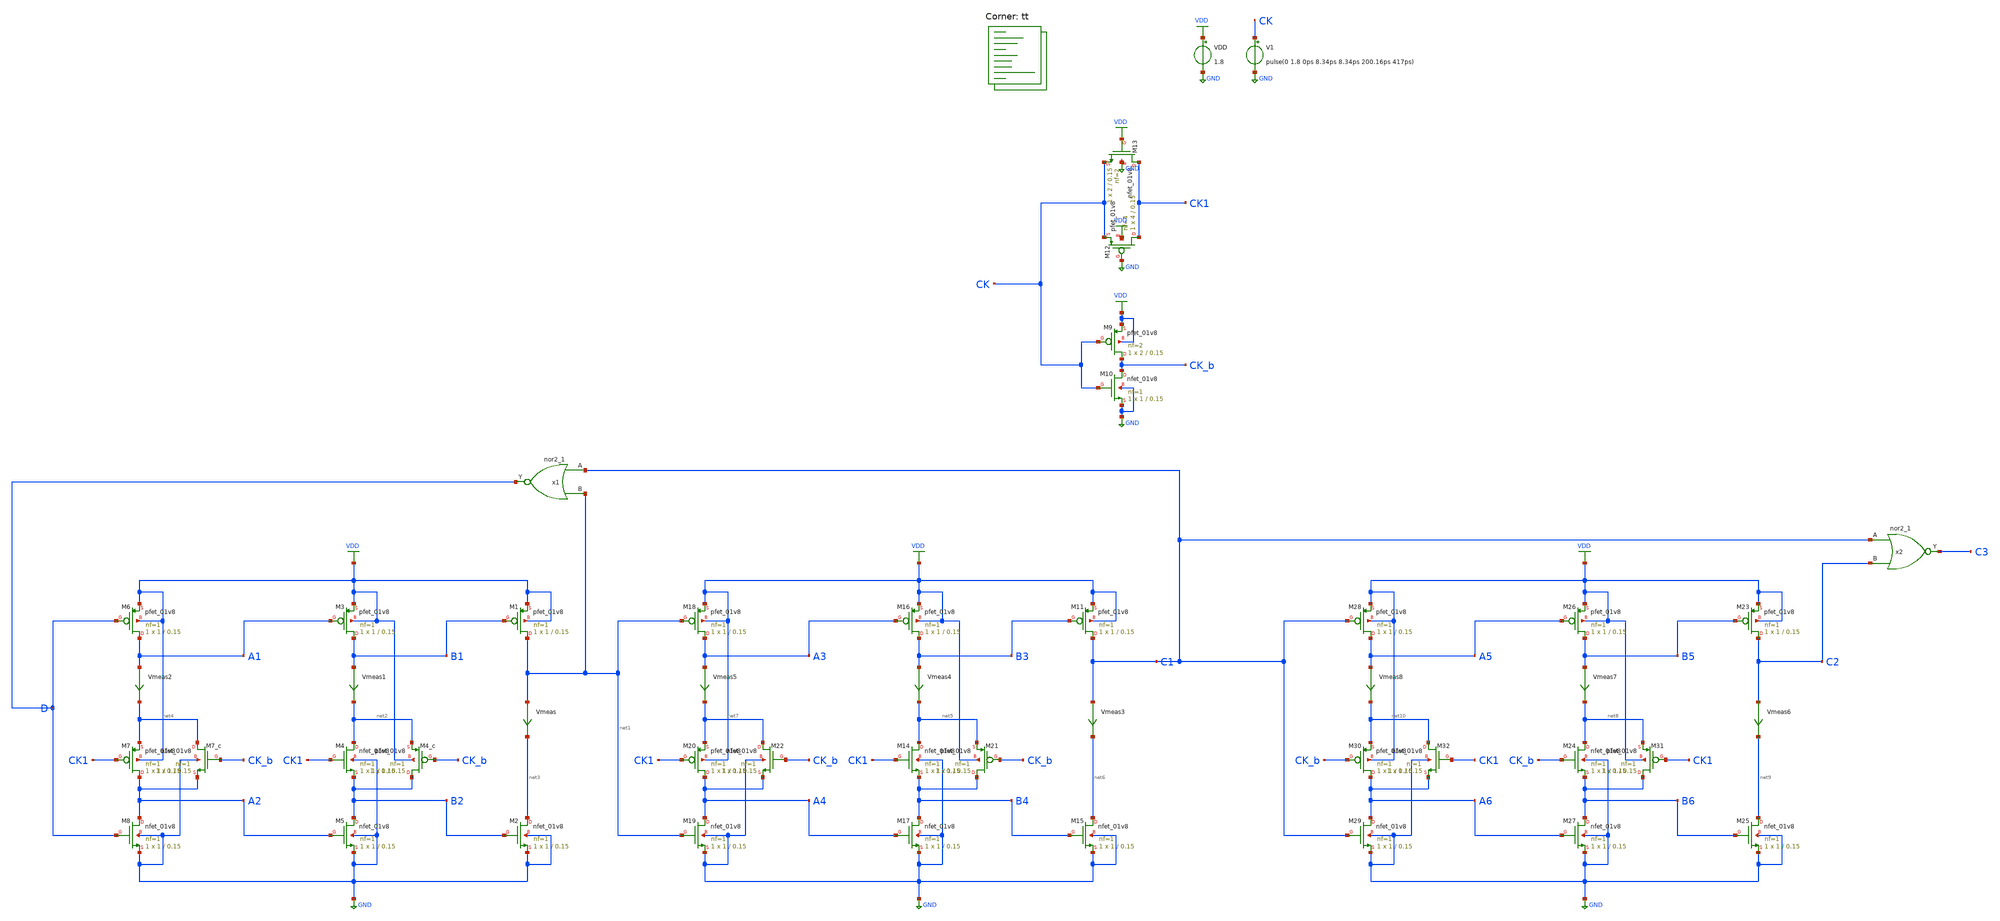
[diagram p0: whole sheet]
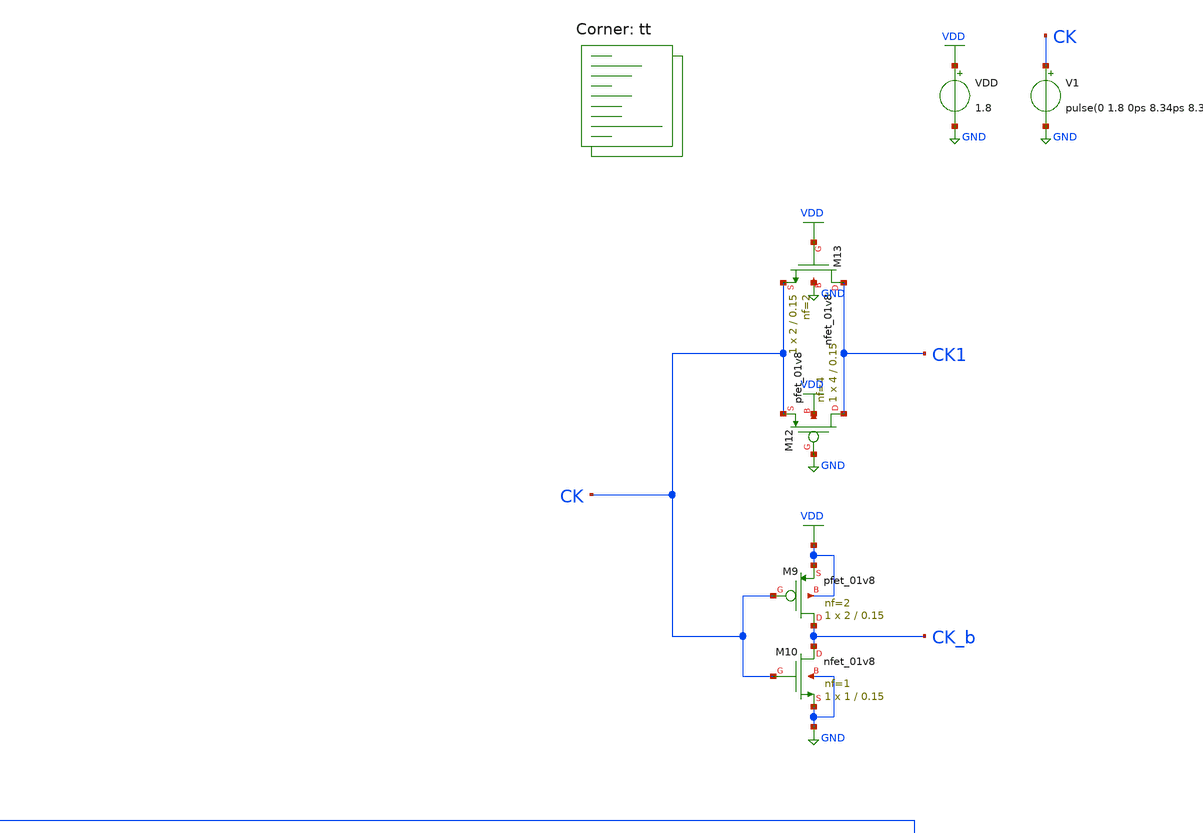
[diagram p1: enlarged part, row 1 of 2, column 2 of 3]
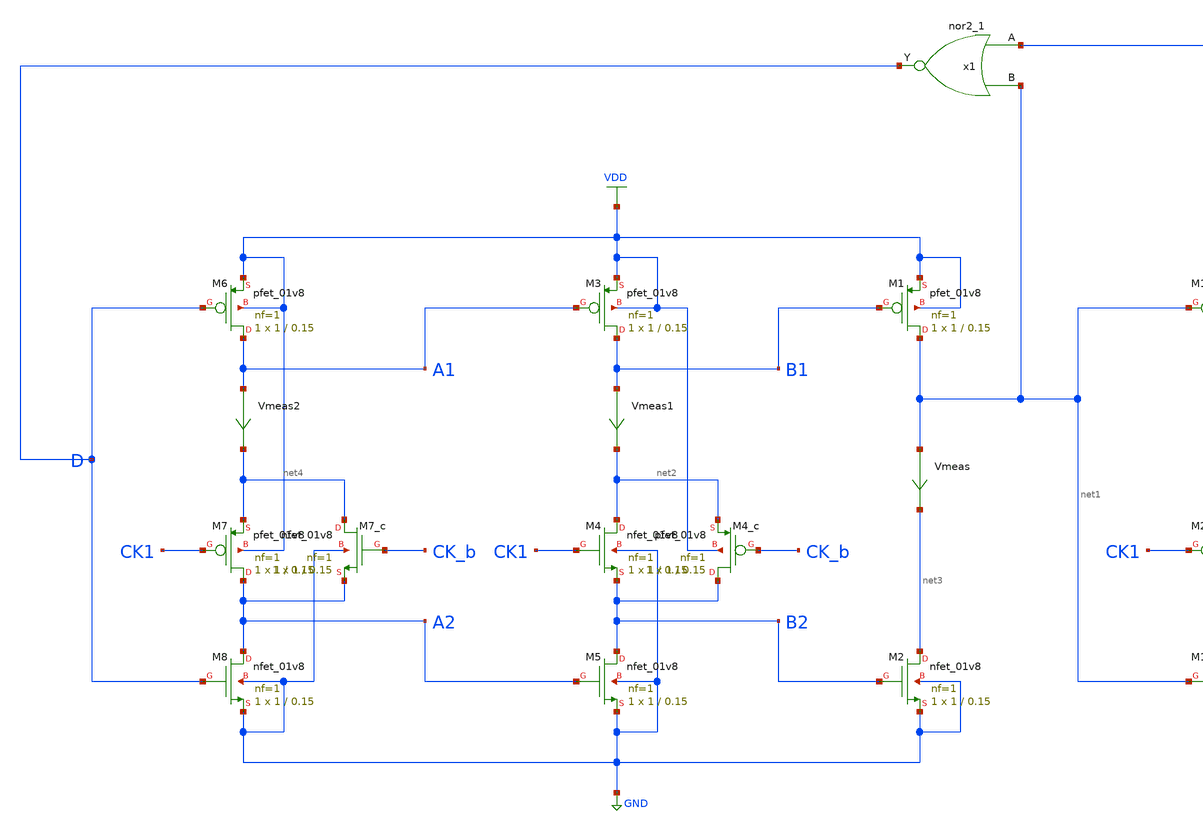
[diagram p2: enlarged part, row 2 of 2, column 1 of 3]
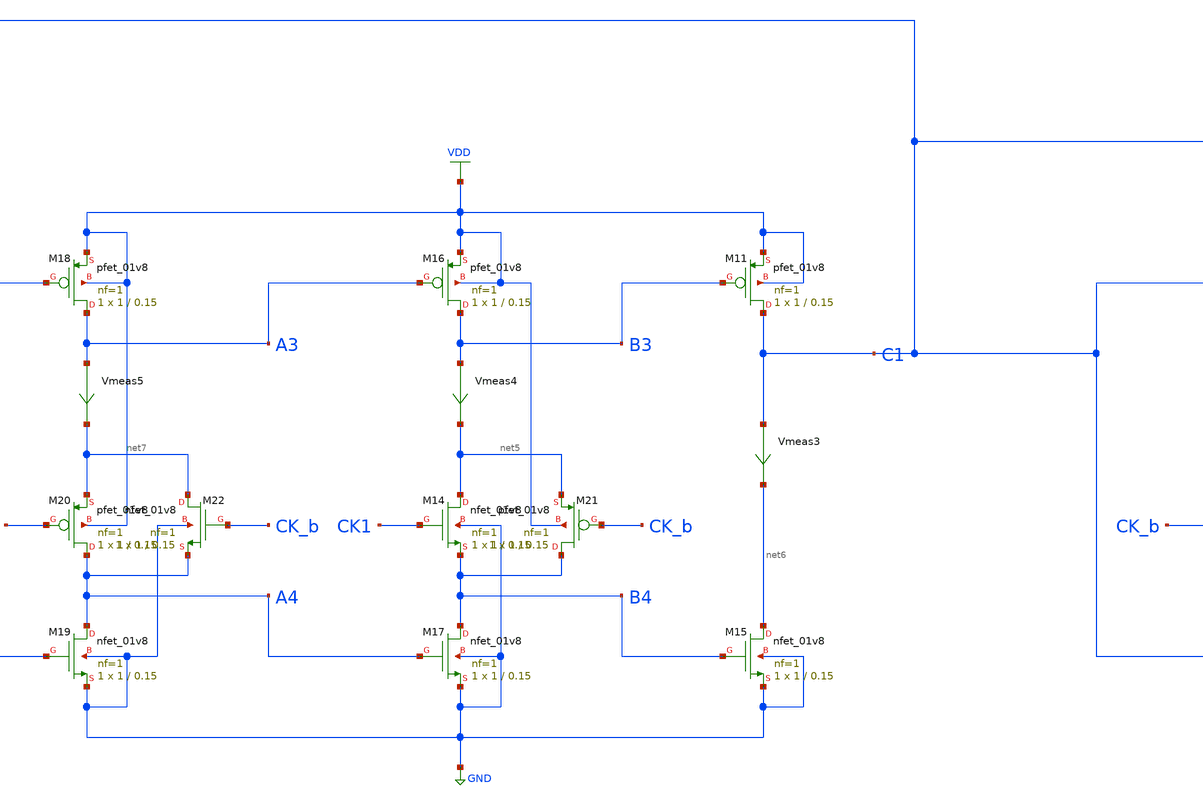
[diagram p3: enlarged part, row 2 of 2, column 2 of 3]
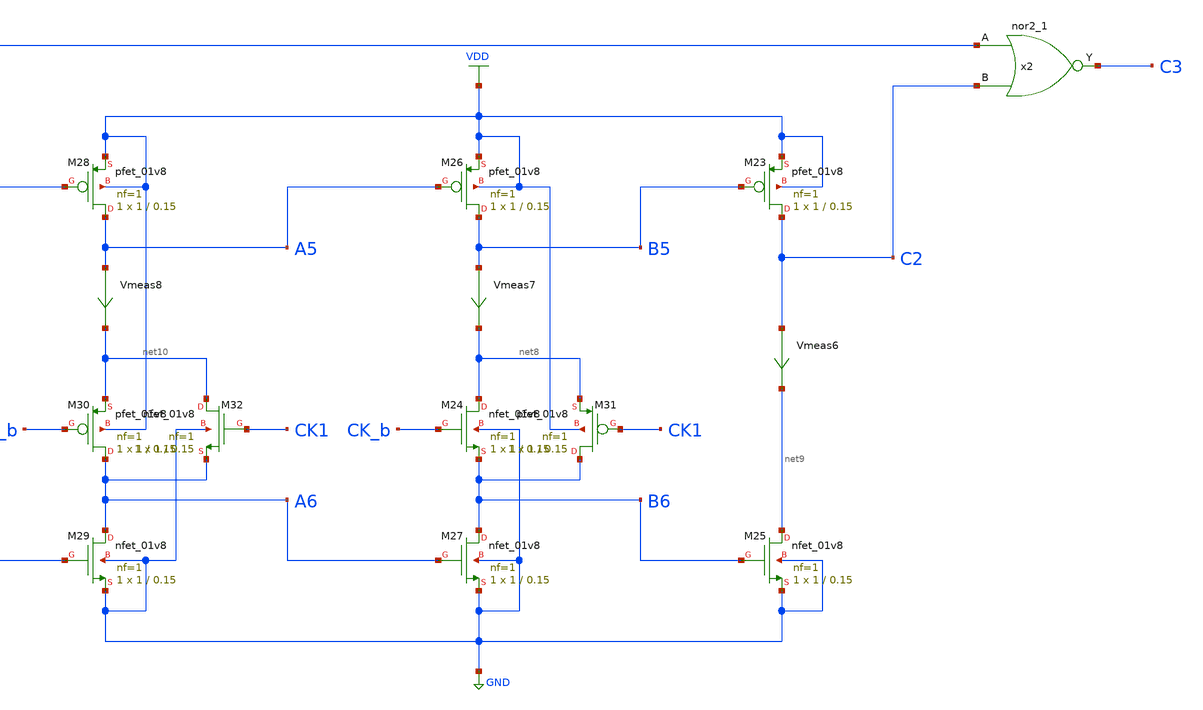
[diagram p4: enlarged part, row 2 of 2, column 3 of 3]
** sch_path: projects/pll/divider/xschem_ngspice/tb_TSPC_FF_comp_sw_divide3.sch
**.subckt tb_TSPC_FF_comp_sw_divide3
VDD VDD GND 1.8
XM1 net1 B1 VDD VDD sky130_fd_pr__pfet_01v8 L=0.15 W=1 nf=1 ad='int((nf+1)/2) * W/nf * 0.29' as='int((nf+2)/2) * W/nf * 0.29'
+ pd='2*int((nf+1)/2) * (W/nf + 0.29)' ps='2*int((nf+2)/2) * (W/nf + 0.29)' nrd='0.29 / W' nrs='0.29 / W'
+ sa=0 sb=0 sd=0 mult=1 m=1
XM4 net2 CK1 B2 GND sky130_fd_pr__nfet_01v8 L=0.15 W=1 nf=1 ad='int((nf+1)/2) * W/nf * 0.29' as='int((nf+2)/2) * W/nf * 0.29'
+ pd='2*int((nf+1)/2) * (W/nf + 0.29)' ps='2*int((nf+2)/2) * (W/nf + 0.29)' nrd='0.29 / W' nrs='0.29 / W'
+ sa=0 sb=0 sd=0 mult=1 m=1
Vmeas net1 net3 0
.save i(vmeas)
XM2 net3 B2 GND GND sky130_fd_pr__nfet_01v8 L=0.15 W=1 nf=1 ad='int((nf+1)/2) * W/nf * 0.29' as='int((nf+2)/2) * W/nf * 0.29'
+ pd='2*int((nf+1)/2) * (W/nf + 0.29)' ps='2*int((nf+2)/2) * (W/nf + 0.29)' nrd='0.29 / W' nrs='0.29 / W'
+ sa=0 sb=0 sd=0 mult=1 m=1
XM3 B1 A1 VDD VDD sky130_fd_pr__pfet_01v8 L=0.15 W=1 nf=1 ad='int((nf+1)/2) * W/nf * 0.29' as='int((nf+2)/2) * W/nf * 0.29'
+ pd='2*int((nf+1)/2) * (W/nf + 0.29)' ps='2*int((nf+2)/2) * (W/nf + 0.29)' nrd='0.29 / W' nrs='0.29 / W'
+ sa=0 sb=0 sd=0 mult=1 m=1
XM5 B2 A2 GND GND sky130_fd_pr__nfet_01v8 L=0.15 W=1 nf=1 ad='int((nf+1)/2) * W/nf * 0.29' as='int((nf+2)/2) * W/nf * 0.29'
+ pd='2*int((nf+1)/2) * (W/nf + 0.29)' ps='2*int((nf+2)/2) * (W/nf + 0.29)' nrd='0.29 / W' nrs='0.29 / W'
+ sa=0 sb=0 sd=0 mult=1 m=1
Vmeas1 B1 net2 0
.save i(vmeas1)
XM6 A1 D VDD VDD sky130_fd_pr__pfet_01v8 L=0.15 W=1 nf=1 ad='int((nf+1)/2) * W/nf * 0.29' as='int((nf+2)/2) * W/nf * 0.29'
+ pd='2*int((nf+1)/2) * (W/nf + 0.29)' ps='2*int((nf+2)/2) * (W/nf + 0.29)' nrd='0.29 / W' nrs='0.29 / W'
+ sa=0 sb=0 sd=0 mult=1 m=1
XM8 A2 D GND GND sky130_fd_pr__nfet_01v8 L=0.15 W=1 nf=1 ad='int((nf+1)/2) * W/nf * 0.29' as='int((nf+2)/2) * W/nf * 0.29'
+ pd='2*int((nf+1)/2) * (W/nf + 0.29)' ps='2*int((nf+2)/2) * (W/nf + 0.29)' nrd='0.29 / W' nrs='0.29 / W'
+ sa=0 sb=0 sd=0 mult=1 m=1
Vmeas2 A1 net4 0
.save i(vmeas2)
XM7 A2 CK1 net4 VDD sky130_fd_pr__pfet_01v8 L=0.15 W=1 nf=1 ad='int((nf+1)/2) * W/nf * 0.29' as='int((nf+2)/2) * W/nf * 0.29'
+ pd='2*int((nf+1)/2) * (W/nf + 0.29)' ps='2*int((nf+2)/2) * (W/nf + 0.29)' nrd='0.29 / W' nrs='0.29 / W'
+ sa=0 sb=0 sd=0 mult=1 m=1
XM4_c B2 CK_b net2 VDD sky130_fd_pr__pfet_01v8 L=0.15 W=1 nf=1 ad='int((nf+1)/2) * W/nf * 0.29' as='int((nf+2)/2) * W/nf * 0.29'
+ pd='2*int((nf+1)/2) * (W/nf + 0.29)' ps='2*int((nf+2)/2) * (W/nf + 0.29)' nrd='0.29 / W' nrs='0.29 / W'
+ sa=0 sb=0 sd=0 mult=1 m=1
XM7_c net4 CK_b A2 GND sky130_fd_pr__nfet_01v8 L=0.15 W=1 nf=1 ad='int((nf+1)/2) * W/nf * 0.29' as='int((nf+2)/2) * W/nf * 0.29'
+ pd='2*int((nf+1)/2) * (W/nf + 0.29)' ps='2*int((nf+2)/2) * (W/nf + 0.29)' nrd='0.29 / W' nrs='0.29 / W'
+ sa=0 sb=0 sd=0 mult=1 m=1
XM12 CK1 GND CK VDD sky130_fd_pr__pfet_01v8 L=0.15 W=4 nf=4 ad='int((nf+1)/2) * W/nf * 0.29' as='int((nf+2)/2) * W/nf * 0.29'
+ pd='2*int((nf+1)/2) * (W/nf + 0.29)' ps='2*int((nf+2)/2) * (W/nf + 0.29)' nrd='0.29 / W' nrs='0.29 / W'
+ sa=0 sb=0 sd=0 mult=1 m=1
XM13 CK1 VDD CK GND sky130_fd_pr__nfet_01v8 L=0.15 W=2 nf=2 ad='int((nf+1)/2) * W/nf * 0.29' as='int((nf+2)/2) * W/nf * 0.29'
+ pd='2*int((nf+1)/2) * (W/nf + 0.29)' ps='2*int((nf+2)/2) * (W/nf + 0.29)' nrd='0.29 / W' nrs='0.29 / W'
+ sa=0 sb=0 sd=0 mult=1 m=1
XM9 CK_b CK VDD VDD sky130_fd_pr__pfet_01v8 L=0.15 W=2 nf=2 ad='int((nf+1)/2) * W/nf * 0.29' as='int((nf+2)/2) * W/nf * 0.29'
+ pd='2*int((nf+1)/2) * (W/nf + 0.29)' ps='2*int((nf+2)/2) * (W/nf + 0.29)' nrd='0.29 / W' nrs='0.29 / W'
+ sa=0 sb=0 sd=0 mult=1 m=1
XM10 CK_b CK GND GND sky130_fd_pr__nfet_01v8 L=0.15 W=1 nf=1 ad='int((nf+1)/2) * W/nf * 0.29' as='int((nf+2)/2) * W/nf * 0.29'
+ pd='2*int((nf+1)/2) * (W/nf + 0.29)' ps='2*int((nf+2)/2) * (W/nf + 0.29)' nrd='0.29 / W' nrs='0.29 / W'
+ sa=0 sb=0 sd=0 mult=1 m=1
V1 CK GND pulse(0 1.8 0ps 8.34ps 8.34ps 200.16ps 417ps)
XM11 C1 B3 VDD VDD sky130_fd_pr__pfet_01v8 L=0.15 W=1 nf=1 ad='int((nf+1)/2) * W/nf * 0.29' as='int((nf+2)/2) * W/nf * 0.29'
+ pd='2*int((nf+1)/2) * (W/nf + 0.29)' ps='2*int((nf+2)/2) * (W/nf + 0.29)' nrd='0.29 / W' nrs='0.29 / W'
+ sa=0 sb=0 sd=0 mult=1 m=1
XM14 net5 CK1 B4 GND sky130_fd_pr__nfet_01v8 L=0.15 W=1 nf=1 ad='int((nf+1)/2) * W/nf * 0.29' as='int((nf+2)/2) * W/nf * 0.29'
+ pd='2*int((nf+1)/2) * (W/nf + 0.29)' ps='2*int((nf+2)/2) * (W/nf + 0.29)' nrd='0.29 / W' nrs='0.29 / W'
+ sa=0 sb=0 sd=0 mult=1 m=1
Vmeas3 C1 net6 0
.save i(vmeas3)
XM15 net6 B4 GND GND sky130_fd_pr__nfet_01v8 L=0.15 W=1 nf=1 ad='int((nf+1)/2) * W/nf * 0.29' as='int((nf+2)/2) * W/nf * 0.29'
+ pd='2*int((nf+1)/2) * (W/nf + 0.29)' ps='2*int((nf+2)/2) * (W/nf + 0.29)' nrd='0.29 / W' nrs='0.29 / W'
+ sa=0 sb=0 sd=0 mult=1 m=1
XM16 B3 A3 VDD VDD sky130_fd_pr__pfet_01v8 L=0.15 W=1 nf=1 ad='int((nf+1)/2) * W/nf * 0.29' as='int((nf+2)/2) * W/nf * 0.29'
+ pd='2*int((nf+1)/2) * (W/nf + 0.29)' ps='2*int((nf+2)/2) * (W/nf + 0.29)' nrd='0.29 / W' nrs='0.29 / W'
+ sa=0 sb=0 sd=0 mult=1 m=1
XM17 B4 A4 GND GND sky130_fd_pr__nfet_01v8 L=0.15 W=1 nf=1 ad='int((nf+1)/2) * W/nf * 0.29' as='int((nf+2)/2) * W/nf * 0.29'
+ pd='2*int((nf+1)/2) * (W/nf + 0.29)' ps='2*int((nf+2)/2) * (W/nf + 0.29)' nrd='0.29 / W' nrs='0.29 / W'
+ sa=0 sb=0 sd=0 mult=1 m=1
Vmeas4 B3 net5 0
.save i(vmeas4)
XM18 A3 net1 VDD VDD sky130_fd_pr__pfet_01v8 L=0.15 W=1 nf=1 ad='int((nf+1)/2) * W/nf * 0.29' as='int((nf+2)/2) * W/nf * 0.29'
+ pd='2*int((nf+1)/2) * (W/nf + 0.29)' ps='2*int((nf+2)/2) * (W/nf + 0.29)' nrd='0.29 / W' nrs='0.29 / W'
+ sa=0 sb=0 sd=0 mult=1 m=1
XM19 A4 net1 GND GND sky130_fd_pr__nfet_01v8 L=0.15 W=1 nf=1 ad='int((nf+1)/2) * W/nf * 0.29' as='int((nf+2)/2) * W/nf * 0.29'
+ pd='2*int((nf+1)/2) * (W/nf + 0.29)' ps='2*int((nf+2)/2) * (W/nf + 0.29)' nrd='0.29 / W' nrs='0.29 / W'
+ sa=0 sb=0 sd=0 mult=1 m=1
Vmeas5 A3 net7 0
.save i(vmeas5)
XM20 A4 CK1 net7 VDD sky130_fd_pr__pfet_01v8 L=0.15 W=1 nf=1 ad='int((nf+1)/2) * W/nf * 0.29' as='int((nf+2)/2) * W/nf * 0.29'
+ pd='2*int((nf+1)/2) * (W/nf + 0.29)' ps='2*int((nf+2)/2) * (W/nf + 0.29)' nrd='0.29 / W' nrs='0.29 / W'
+ sa=0 sb=0 sd=0 mult=1 m=1
XM21 B4 CK_b net5 VDD sky130_fd_pr__pfet_01v8 L=0.15 W=1 nf=1 ad='int((nf+1)/2) * W/nf * 0.29' as='int((nf+2)/2) * W/nf * 0.29'
+ pd='2*int((nf+1)/2) * (W/nf + 0.29)' ps='2*int((nf+2)/2) * (W/nf + 0.29)' nrd='0.29 / W' nrs='0.29 / W'
+ sa=0 sb=0 sd=0 mult=1 m=1
XM22 net7 CK_b A4 GND sky130_fd_pr__nfet_01v8 L=0.15 W=1 nf=1 ad='int((nf+1)/2) * W/nf * 0.29' as='int((nf+2)/2) * W/nf * 0.29'
+ pd='2*int((nf+1)/2) * (W/nf + 0.29)' ps='2*int((nf+2)/2) * (W/nf + 0.29)' nrd='0.29 / W' nrs='0.29 / W'
+ sa=0 sb=0 sd=0 mult=1 m=1
XM23 C2 B5 VDD VDD sky130_fd_pr__pfet_01v8 L=0.15 W=1 nf=1 ad='int((nf+1)/2) * W/nf * 0.29' as='int((nf+2)/2) * W/nf * 0.29'
+ pd='2*int((nf+1)/2) * (W/nf + 0.29)' ps='2*int((nf+2)/2) * (W/nf + 0.29)' nrd='0.29 / W' nrs='0.29 / W'
+ sa=0 sb=0 sd=0 mult=1 m=1
XM24 net8 CK_b B6 GND sky130_fd_pr__nfet_01v8 L=0.15 W=1 nf=1 ad='int((nf+1)/2) * W/nf * 0.29' as='int((nf+2)/2) * W/nf * 0.29'
+ pd='2*int((nf+1)/2) * (W/nf + 0.29)' ps='2*int((nf+2)/2) * (W/nf + 0.29)' nrd='0.29 / W' nrs='0.29 / W'
+ sa=0 sb=0 sd=0 mult=1 m=1
Vmeas6 C2 net9 0
.save i(vmeas6)
XM25 net9 B6 GND GND sky130_fd_pr__nfet_01v8 L=0.15 W=1 nf=1 ad='int((nf+1)/2) * W/nf * 0.29' as='int((nf+2)/2) * W/nf * 0.29'
+ pd='2*int((nf+1)/2) * (W/nf + 0.29)' ps='2*int((nf+2)/2) * (W/nf + 0.29)' nrd='0.29 / W' nrs='0.29 / W'
+ sa=0 sb=0 sd=0 mult=1 m=1
XM26 B5 A5 VDD VDD sky130_fd_pr__pfet_01v8 L=0.15 W=1 nf=1 ad='int((nf+1)/2) * W/nf * 0.29' as='int((nf+2)/2) * W/nf * 0.29'
+ pd='2*int((nf+1)/2) * (W/nf + 0.29)' ps='2*int((nf+2)/2) * (W/nf + 0.29)' nrd='0.29 / W' nrs='0.29 / W'
+ sa=0 sb=0 sd=0 mult=1 m=1
XM27 B6 A6 GND GND sky130_fd_pr__nfet_01v8 L=0.15 W=1 nf=1 ad='int((nf+1)/2) * W/nf * 0.29' as='int((nf+2)/2) * W/nf * 0.29'
+ pd='2*int((nf+1)/2) * (W/nf + 0.29)' ps='2*int((nf+2)/2) * (W/nf + 0.29)' nrd='0.29 / W' nrs='0.29 / W'
+ sa=0 sb=0 sd=0 mult=1 m=1
Vmeas7 B5 net8 0
.save i(vmeas7)
XM28 A5 C1 VDD VDD sky130_fd_pr__pfet_01v8 L=0.15 W=1 nf=1 ad='int((nf+1)/2) * W/nf * 0.29' as='int((nf+2)/2) * W/nf * 0.29'
+ pd='2*int((nf+1)/2) * (W/nf + 0.29)' ps='2*int((nf+2)/2) * (W/nf + 0.29)' nrd='0.29 / W' nrs='0.29 / W'
+ sa=0 sb=0 sd=0 mult=1 m=1
XM29 A6 C1 GND GND sky130_fd_pr__nfet_01v8 L=0.15 W=1 nf=1 ad='int((nf+1)/2) * W/nf * 0.29' as='int((nf+2)/2) * W/nf * 0.29'
+ pd='2*int((nf+1)/2) * (W/nf + 0.29)' ps='2*int((nf+2)/2) * (W/nf + 0.29)' nrd='0.29 / W' nrs='0.29 / W'
+ sa=0 sb=0 sd=0 mult=1 m=1
Vmeas8 A5 net10 0
.save i(vmeas8)
XM30 A6 CK_b net10 VDD sky130_fd_pr__pfet_01v8 L=0.15 W=1 nf=1 ad='int((nf+1)/2) * W/nf * 0.29' as='int((nf+2)/2) * W/nf * 0.29'
+ pd='2*int((nf+1)/2) * (W/nf + 0.29)' ps='2*int((nf+2)/2) * (W/nf + 0.29)' nrd='0.29 / W' nrs='0.29 / W'
+ sa=0 sb=0 sd=0 mult=1 m=1
XM31 B6 CK1 net8 VDD sky130_fd_pr__pfet_01v8 L=0.15 W=1 nf=1 ad='int((nf+1)/2) * W/nf * 0.29' as='int((nf+2)/2) * W/nf * 0.29'
+ pd='2*int((nf+1)/2) * (W/nf + 0.29)' ps='2*int((nf+2)/2) * (W/nf + 0.29)' nrd='0.29 / W' nrs='0.29 / W'
+ sa=0 sb=0 sd=0 mult=1 m=1
XM32 net10 CK1 A6 GND sky130_fd_pr__nfet_01v8 L=0.15 W=1 nf=1 ad='int((nf+1)/2) * W/nf * 0.29' as='int((nf+2)/2) * W/nf * 0.29'
+ pd='2*int((nf+1)/2) * (W/nf + 0.29)' ps='2*int((nf+2)/2) * (W/nf + 0.29)' nrd='0.29 / W' nrs='0.29 / W'
+ sa=0 sb=0 sd=0 mult=1 m=1
x1 C1 net1 VGND VNB VPB VPWR D sky130_fd_sc_hd__nor2_1
x2 C1 C2 VGND VNB VPB VPWR C3 sky130_fd_sc_hd__nor2_1
**** begin user architecture code



.include /foss/pdks/sky130A/libs.ref/sky130_fd_sc_hd/spice/sky130_fd_sc_hd.spice

.option method=gear
.option wnflag=1
.option savecurrents

.save @m.xm1.msky130_fd_pr__pfet_01v8[gm] @m.xm2.msky130_fd_pr__nfet_01v8[gm] @m.xm3.msky130_fd_pr__pfet_01v8[gm] @m.xm4.msky130_fd_pr__nfet_01v8[gm] @m.xm4_c.msky130_fd_pr__pfet_01v8[gm] @m.xm5.msky130_fd_pr__nfet_01v8[gm] @m.xm6.msky130_fd_pr__pfet_01v8[gm] @m.xm7.msky130_fd_pr__pfet_01v8[gm] @m.xm7_c.msky130_fd_pr__nfet_01v8[gm] @m.xm8.msky130_fd_pr__nfet_01v8[gm]


.control

  save v(d) v(a1) v(a2) v(a3) v(a4) v(a5) v(a6) v(b1) v(b2) v(b3) v(b4) v(b5) v(b6) v(c) v(c1) v(c2)
+ v(c3) v(ck) v(ck_b) v(vdd) v(gnd)
  * save all
  * tran 0.1n 1u
  tran 0.2p 10n

  remzerovec
  write tb_TSPC_FF_comp_sw_divide3.raw
  set appendwrite

.endc



.lib $::SKYWATER_MODELS/sky130.lib.spice tt
**** end user architecture code
**.ends
.GLOBAL GND
.GLOBAL VDD
.end
